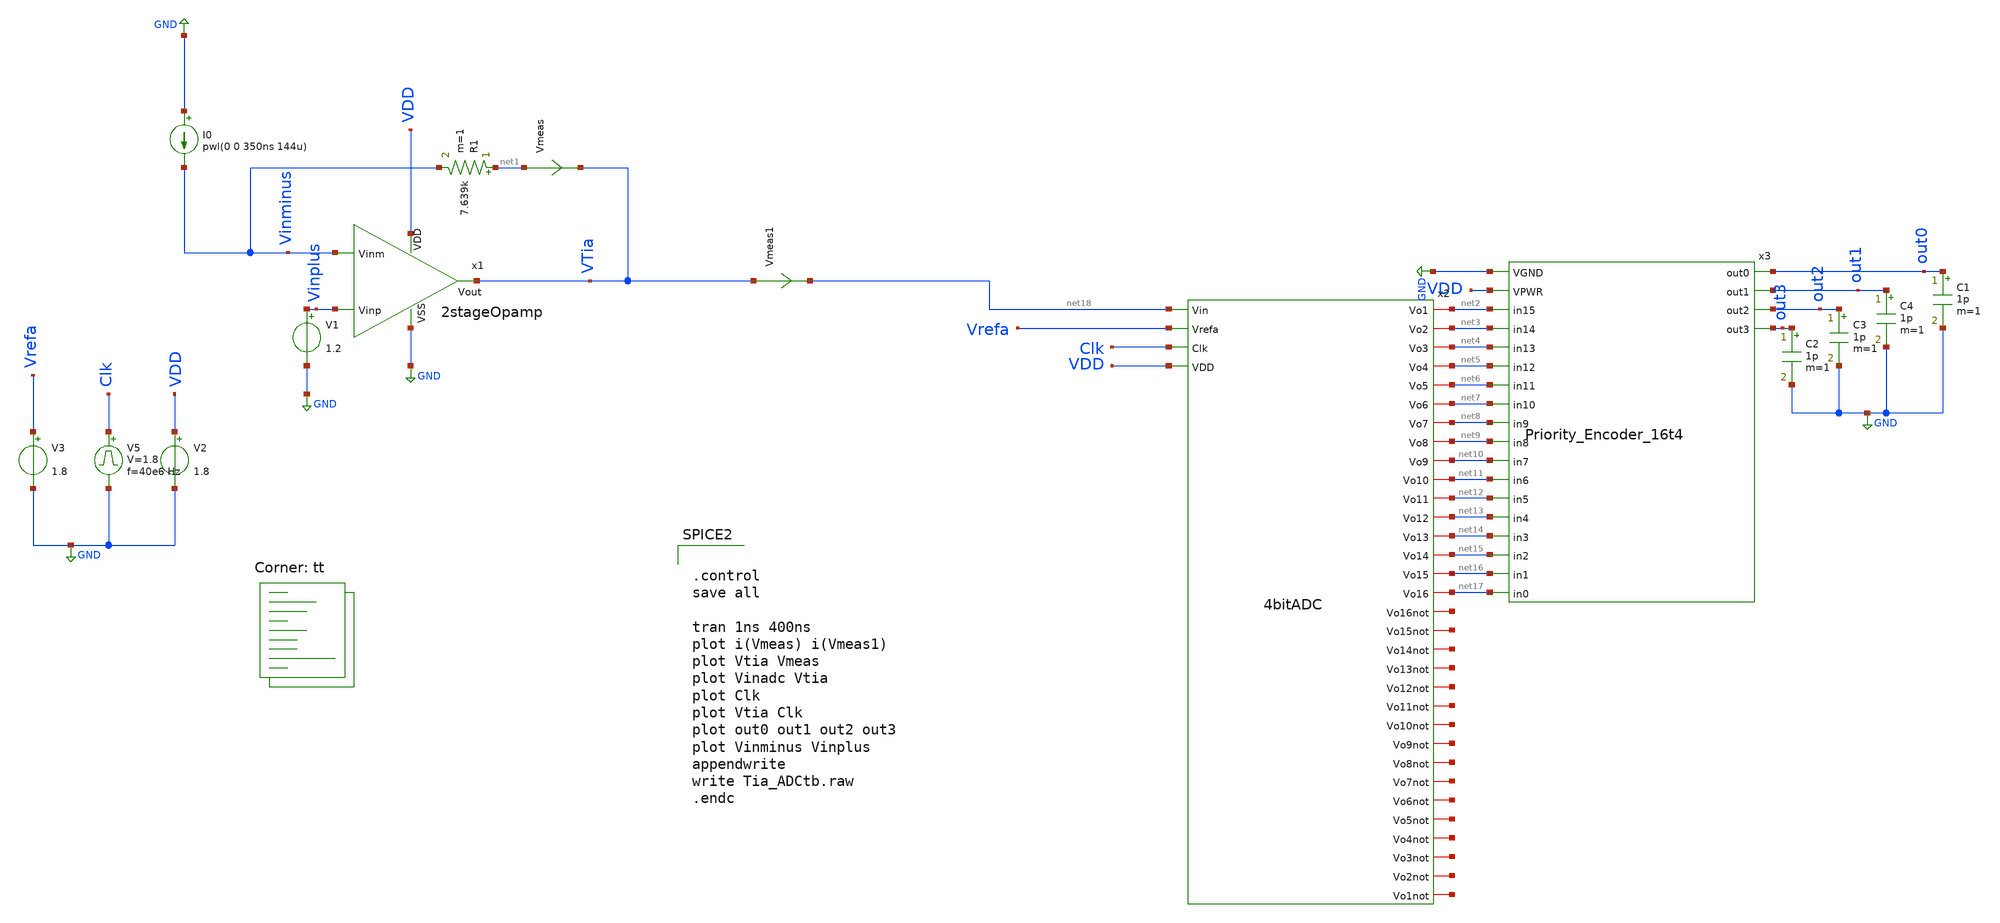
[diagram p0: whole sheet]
** sch_path: userLib/userLib/Tia_ADCtb.sch
**.subckt Tia_ADCtb
I0 GND Vinminus pwl(0 0 350ns 144u)
R1 net1 Vinminus 7.639k m=1
V1 Vinplus GND 1.2
Vmeas net1 VTia 0
.save i(vmeas)
V2 VDD GND 1.8
V3 Vrefa GND 1.8
.save i(v3)
V5 Clk GND pulse 0 1.8 '0.495/ 40e6 ' '0.01/40e6 ' '0.01/40e6 ' '0.49/40e6 ' '1/40e6 '
C1 out0 GND 1p m=1
C2 out3 GND 1p m=1
C3 out2 GND 1p m=1
C4 out1 GND 1p m=1
Vmeas1 VTia net18 0
.save i(vmeas1)
x1 VDD Vinminus Vinplus VTia GND 2stageOpamp
x2 net2 net3 net18 net4 Vrefa net5 net6 Clk net7 net8 VDD net9 net10 net11 net12 net13 net14 net15
+ net16 net17 net19 net20 net21 net22 net23 net24 net25 net26 net27 net28 net29 net30 net31 net32 net33
+ net34 4bitADC
x3 GND VDD net17 net16 net7 net6 net5 net4 net3 net2 net15 net14 net13 net12 net11 net10 net9 net8
+ out0 out1 out2 out3 Priority_Encoder_16t4
**** begin user architecture code
.lib $::SKYWATER_MODELS/sky130.lib.spice tt


.control
save all

tran 1ns 400ns
plot i(Vmeas) i(Vmeas1)
plot Vtia Vmeas
plot Vinadc Vtia
plot Clk
plot Vtia Clk
plot out0 out1 out2 out3
plot Vinminus Vinplus
appendwrite
write Tia_ADCtb.raw
.endc



** opencircuitdesign pdks install
.include $::SKYWATER_STDCELLS/sky130_fd_sc_hd.spice


**** end user architecture code
**.ends
.GLOBAL GND
.end
